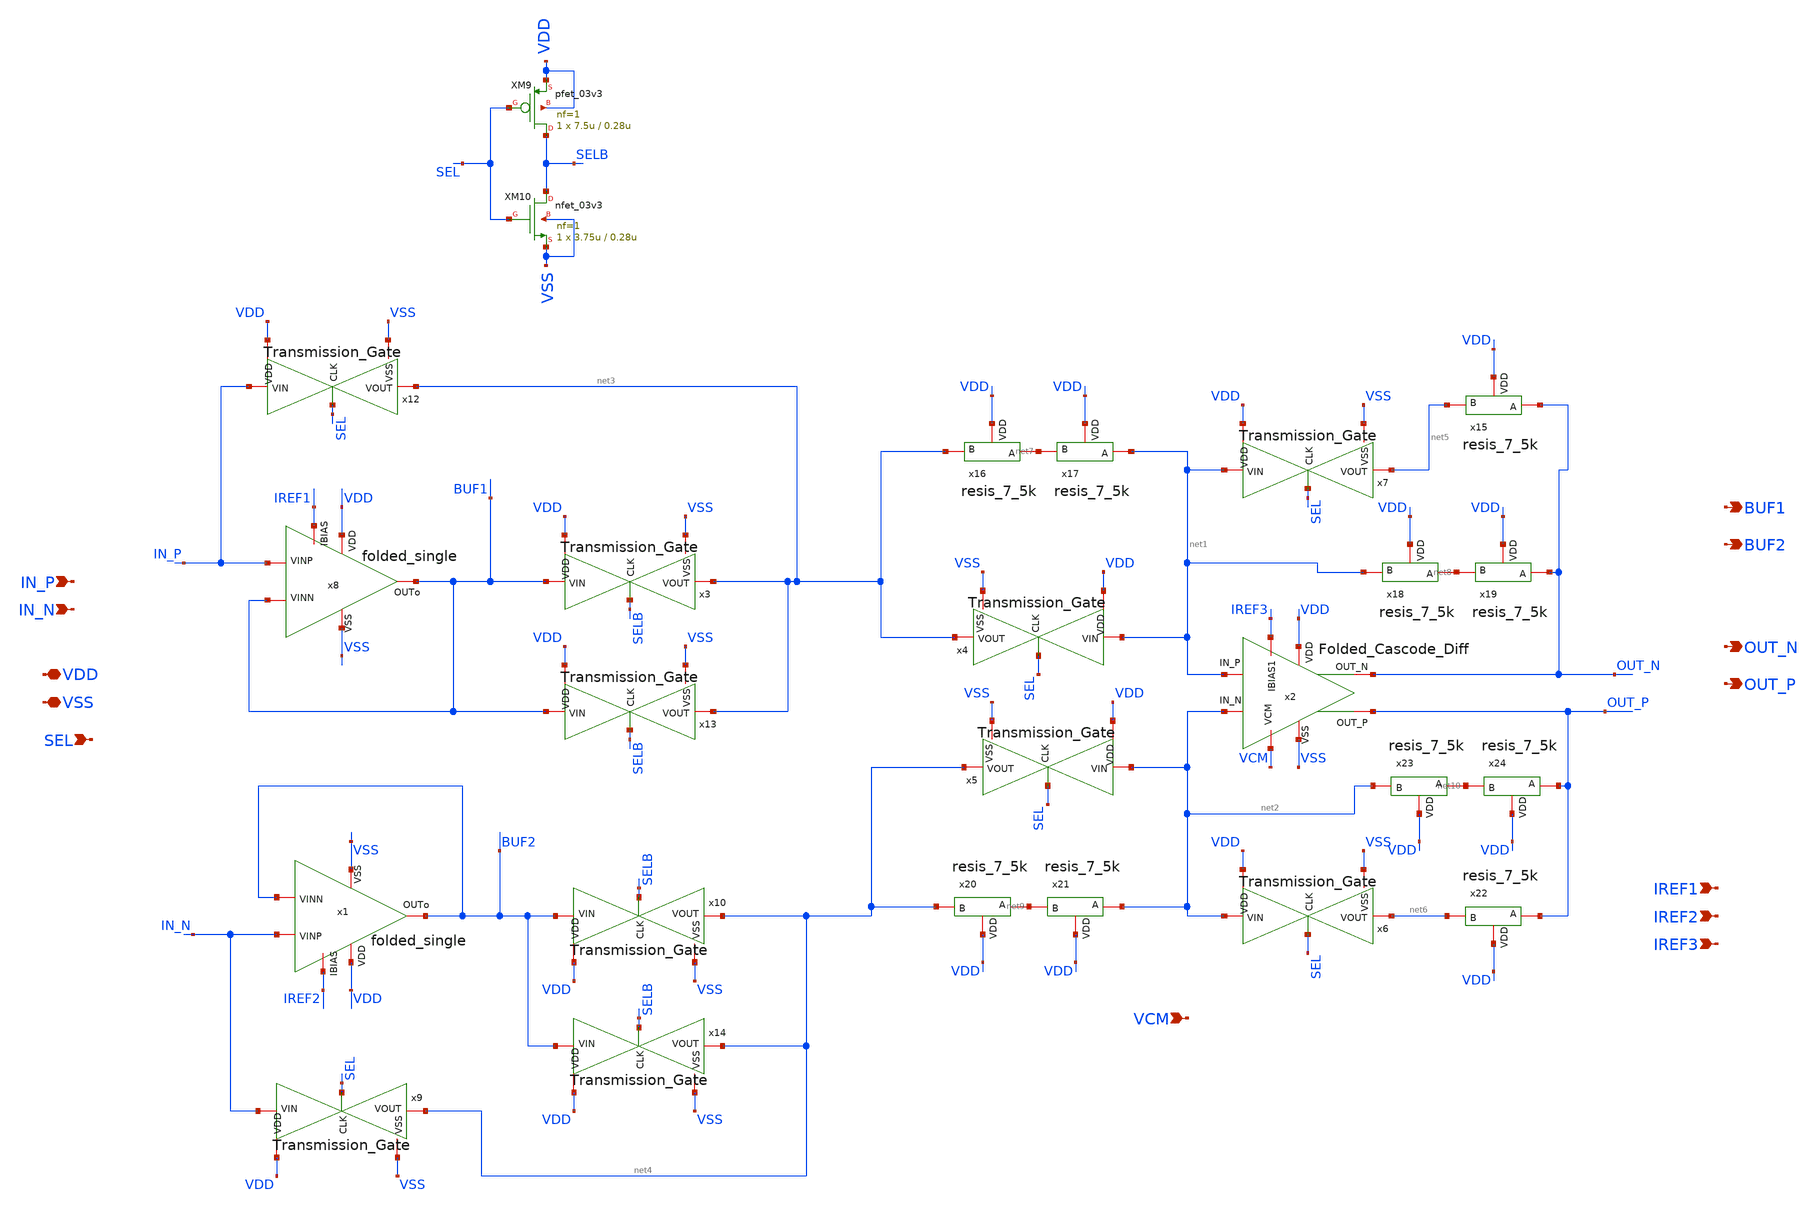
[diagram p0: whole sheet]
** sch_path: SCOP_INPUT_AND_MUX_PAKISTAN_03/Xschem/TransImpedance/transimpedence_block.sch
**.subckt transimpedence_block IN_P IN_N VDD VSS IREF1 SEL OUT_N OUT_P VCM IREF2 IREF3 BUF1 BUF2
*.ipin IN_P
*.ipin IN_N
*.iopin VDD
*.iopin VSS
*.ipin IREF1
*.ipin SEL
*.opin OUT_N
*.opin OUT_P
*.ipin VCM
*.ipin IREF2
*.ipin IREF3
*.opin BUF1
*.opin BUF2
x3 VDD VSS SELB net3 BUF1 Transmission_Gate
x4 VDD VSS SEL net3 net1 Transmission_Gate
x6 VDD VSS SEL net6 net2 Transmission_Gate
x7 VDD VSS SEL net5 net1 Transmission_Gate
x10 VDD VSS SELB net4 BUF2 Transmission_Gate
x9 VDD VSS SEL net4 IN_N Transmission_Gate
x12 VDD VSS SEL net3 IN_P Transmission_Gate
x5 VDD VSS SEL net4 net2 Transmission_Gate
x13 VDD VSS SELB net3 BUF1 Transmission_Gate
x14 VDD VSS SELB net4 BUF2 Transmission_Gate
x15 OUT_N net5 VDD resis_7_5k
x16 net7 net3 VDD resis_7_5k
x17 net1 net7 VDD resis_7_5k
x18 net8 net1 VDD resis_7_5k
x19 OUT_N net8 VDD resis_7_5k
x20 net9 net4 VDD resis_7_5k
x21 net2 net9 VDD resis_7_5k
x22 OUT_P net6 VDD resis_7_5k
x23 net10 net2 VDD resis_7_5k
x24 OUT_P net10 VDD resis_7_5k
XM9 SELB SEL VDD VDD pfet_03v3 L=0.28u W=7.5u nf=1 ad='int((nf+1)/2) * W/nf * 0.18u' as='int((nf+2)/2) * W/nf * 0.18u'
+ pd='2*int((nf+1)/2) * (W/nf + 0.18u)' ps='2*int((nf+2)/2) * (W/nf + 0.18u)' nrd='0.18u / W' nrs='0.18u / W'
+ sa=0 sb=0 sd=0 m=1
XM10 SELB SEL VSS VSS nfet_03v3 L=0.28u W=3.75u nf=1 ad='int((nf+1)/2) * W/nf * 0.18u' as='int((nf+2)/2) * W/nf * 0.18u'
+ pd='2*int((nf+1)/2) * (W/nf + 0.18u)' ps='2*int((nf+2)/2) * (W/nf + 0.18u)' nrd='0.18u / W' nrs='0.18u / W'
+ sa=0 sb=0 sd=0 m=1
x1 BUF2 IN_N BUF2 VDD VSS IREF2 folded_single
x8 BUF1 IN_P BUF1 VDD VSS IREF1 folded_single
x2 VDD VSS VCM net2 net1 OUT_N OUT_P IREF3 Folded_Cascode_Diff
**.ends
.end
